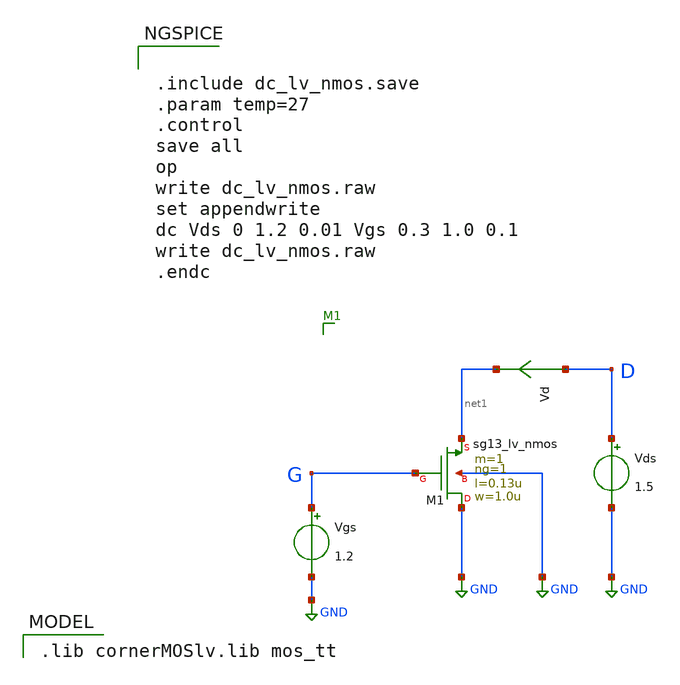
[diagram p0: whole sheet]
** sch_path: ihp-sg13g2/libs.tech/xschem/sg13g2_tests/dc_lv_nmos.sch
* Copyright 2023 IHP PDK Authors
**.subckt dc_lv_nmos
Vgs G GND 1.2
Vds D GND 1.5
Vd D net1 0
.save i(vd)
XM1 GND G net1 GND sg13_lv_nmos w=1.0u l=0.13u ng=1 m=1 mm_ok=1
**** begin user architecture code
 .lib cornerMOSlv.lib mos_tt



.include dc_lv_nmos.save
.param temp=27
.control
save all
op
write dc_lv_nmos.raw
set appendwrite
dc Vds 0 1.2 0.01 Vgs 0.3 1.0 0.1
write dc_lv_nmos.raw
.endc


**** end user architecture code
**.ends
.GLOBAL GND
.end
